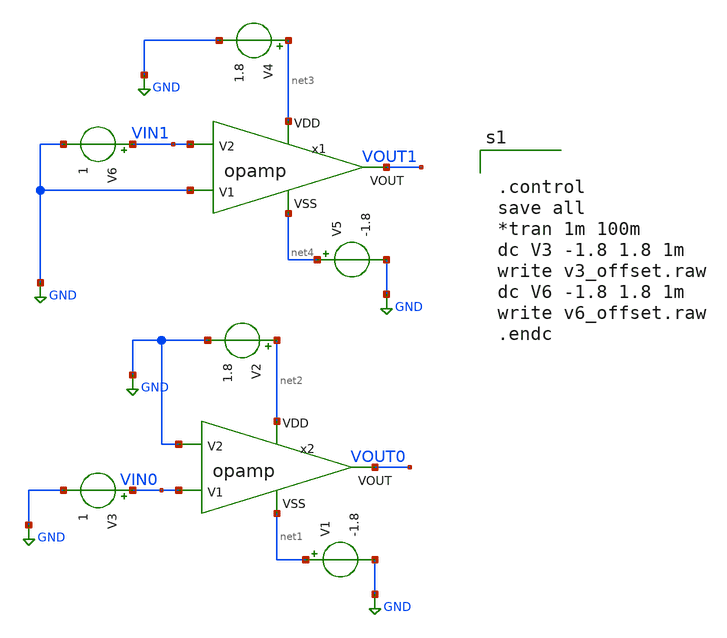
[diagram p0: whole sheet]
** sch_path: opamp_offset.sch
**.subckt opamp_offset
V2 net2 GND 1.8
V1 net1 GND -1.8
V3 VIN0 GND 1
V5 net4 GND -1.8
V6 VIN1 GND 1
V4 net3 GND 1.8
x1 net3 net4 GND VIN1 VOUT1 opamp
x2 net2 net1 VIN0 GND VOUT0 opamp
**** begin user architecture code


.control
save all
*tran 1m 100m
dc V3 -1.8 1.8 1m
write v3_offset.raw
dc V6 -1.8 1.8 1m
write v6_offset.raw
.endc



** opencircuitdesign pdks install
.lib $::SKYWATER_MODELS/sky130.lib.spice tt


**** end user architecture code
**.ends

* expanding   symbol:  /foss/designs/chipalooza2024/sky130_hcmus_ip__instramp/opamp.sym # of pins=5
** sym_path: xschem/opamp.sym
** sch_path: xschem/opamp.sch
.subckt opamp VDD VSS V1 V2 VOUT
*.ipin VSS
*.ipin VDD
*.ipin V2
*.ipin V1
*.opin VOUT
XM2 net4 V2 net1 VSS sky130_fd_pr__nfet_g5v0d10v5 L=1 W=18 nf=1 ad='int((nf+1)/2) * W/nf * 0.29' as='int((nf+2)/2) * W/nf * 0.29'
+ pd='2*int((nf+1)/2) * (W/nf + 0.29)' ps='2*int((nf+2)/2) * (W/nf + 0.29)' nrd='0.29 / W' nrs='0.29 / W'
+ sa=0 sb=0 sd=0 mult=1 m=1
XM1 net5 net4 VDD VDD sky130_fd_pr__pfet_g5v0d10v5 L=1 W=30 nf=1 ad='int((nf+1)/2) * W/nf * 0.29' as='int((nf+2)/2) * W/nf * 0.29'
+ pd='2*int((nf+1)/2) * (W/nf + 0.29)' ps='2*int((nf+2)/2) * (W/nf + 0.29)' nrd='0.29 / W' nrs='0.29 / W'
+ sa=0 sb=0 sd=0 mult=1 m=1
XM4 net5 V1 net1 VSS sky130_fd_pr__nfet_g5v0d10v5 L=1 W=18 nf=1 ad='int((nf+1)/2) * W/nf * 0.29' as='int((nf+2)/2) * W/nf * 0.29'
+ pd='2*int((nf+1)/2) * (W/nf + 0.29)' ps='2*int((nf+2)/2) * (W/nf + 0.29)' nrd='0.29 / W' nrs='0.29 / W'
+ sa=0 sb=0 sd=0 mult=1 m=1
XM5 net1 net6 VSS VSS sky130_fd_pr__nfet_g5v0d10v5 L=1 W=15.171 nf=1 ad='int((nf+1)/2) * W/nf * 0.29'
+ as='int((nf+2)/2) * W/nf * 0.29' pd='2*int((nf+1)/2) * (W/nf + 0.29)' ps='2*int((nf+2)/2) * (W/nf + 0.29)'
+ nrd='0.29 / W' nrs='0.29 / W' sa=0 sb=0 sd=0 mult=1 m=1
XM6 VOUT net6 VSS VSS sky130_fd_pr__nfet_g5v0d10v5 L=1 W=19 nf=1 ad='int((nf+1)/2) * W/nf * 0.29' as='int((nf+2)/2) * W/nf * 0.29'
+ pd='2*int((nf+1)/2) * (W/nf + 0.29)' ps='2*int((nf+2)/2) * (W/nf + 0.29)' nrd='0.29 / W' nrs='0.29 / W'
+ sa=0 sb=0 sd=0 mult=1 m=1
XM7 net6 net6 VSS VSS sky130_fd_pr__nfet_g5v0d10v5 L=1 W=20 nf=1 ad='int((nf+1)/2) * W/nf * 0.29' as='int((nf+2)/2) * W/nf * 0.29'
+ pd='2*int((nf+1)/2) * (W/nf + 0.29)' ps='2*int((nf+2)/2) * (W/nf + 0.29)' nrd='0.29 / W' nrs='0.29 / W'
+ sa=0 sb=0 sd=0 mult=1 m=1
XM3 net4 net4 VDD VDD sky130_fd_pr__pfet_g5v0d10v5 L=1 W=30 nf=1 ad='int((nf+1)/2) * W/nf * 0.29' as='int((nf+2)/2) * W/nf * 0.29'
+ pd='2*int((nf+1)/2) * (W/nf + 0.29)' ps='2*int((nf+2)/2) * (W/nf + 0.29)' nrd='0.29 / W' nrs='0.29 / W'
+ sa=0 sb=0 sd=0 mult=1 m=1
XM8 VOUT net5 VDD VDD sky130_fd_pr__pfet_g5v0d10v5 L=1 W=38 nf=1 ad='int((nf+1)/2) * W/nf * 0.29' as='int((nf+2)/2) * W/nf * 0.29'
+ pd='2*int((nf+1)/2) * (W/nf + 0.29)' ps='2*int((nf+2)/2) * (W/nf + 0.29)' nrd='0.29 / W' nrs='0.29 / W'
+ sa=0 sb=0 sd=0 mult=2 m=2
XC1 net7 net5 sky130_fd_pr__cap_mim_m3_1 W=5.5 L=10 MF=10 m=10
V_ibias net8 net6 0
.save i(v_ibias)
XR5 net2 VDD VSS sky130_fd_pr__res_high_po_0p69 L=18.58 mult=1 m=1
XR1 net3 net2 VSS sky130_fd_pr__res_high_po_0p69 L=18.58 mult=1 m=1
XR2 net8 net3 VSS sky130_fd_pr__res_high_po_0p69 L=18.58 mult=1 m=1
XR3 net7 VOUT VSS sky130_fd_pr__res_high_po_0p69 L=2.41 mult=1 m=1
.ends

.GLOBAL GND
.end
